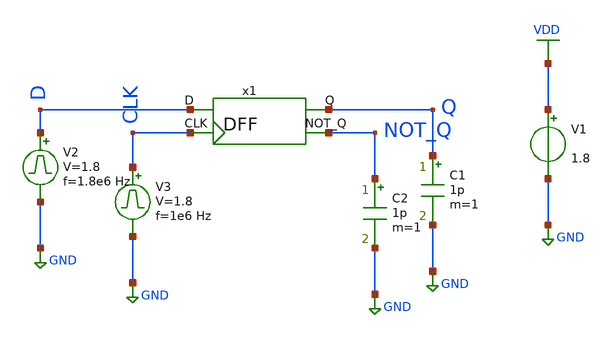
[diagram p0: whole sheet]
** sch_path: library/xschem/DFF_tb.sch
**.subckt DFF_tb
V1 VDD GND 1.8
V2 D GND pulse 0 1.8 '0.495/ 1.8e6 ' '0.01/1.8e6 ' '0.01/1.8e6 ' '0.49/1.8e6 ' '1/1.8e6 '
C1 Q GND 1p m=1
V3 CLK GND pulse 0 1.8 '0.495/ 1e6 ' '0.01/1e6 ' '0.01/1e6 ' '0.49/1e6 ' '1/1e6 '
C2 NOT_Q GND 1p m=1
x1 Q D CLK NOT_Q DFF
**** begin user architecture code


.control
save all
tran 1n 4u
plot V(CLK) V(D)+2 V(Q)+4 V(NOT_Q)+6
.endc


** opencircuitdesign pdks install
.lib $::SKYWATER_MODELS/sky130.lib.spice tt


**** end user architecture code
**.ends

* expanding   symbol:  DFF.sym # of pins=4
** sym_path: library/xschem/DFF.sym
** sch_path: library/xschem/DFF.sch
.subckt DFF Q D CLK NOT_Q
*.ipin D
*.opin Q
*.opin NOT_Q
*.ipin CLK
x1 net2 net1 Q NOT_Q Dlatch
x2 D CLK net2 net3 Dlatch
x3 CLK net1 inv
.ends


* expanding   symbol:  Dlatch.sym # of pins=4
** sym_path: library/xschem/Dlatch.sym
** sch_path: library/xschem/Dlatch.sch
.subckt Dlatch D CLK Q NOT_Q
*.ipin D
*.ipin CLK
*.opin Q
*.opin NOT_Q
XM1 net1 CLK net2 GND sky130_fd_pr__nfet_01v8 L=0.15 W=1 nf=1 ad='int((nf+1)/2) * W/nf * 0.29' as='int((nf+2)/2) * W/nf * 0.29'
+ pd='2*int((nf+1)/2) * (W/nf + 0.29)' ps='2*int((nf+2)/2) * (W/nf + 0.29)' nrd='0.29 / W' nrs='0.29 / W'
+ sa=0 sb=0 sd=0 mult=1 m=1
XM2 net1 D VDD VDD sky130_fd_pr__pfet_01v8 L=0.15 W=1 nf=1 ad='int((nf+1)/2) * W/nf * 0.29' as='int((nf+2)/2) * W/nf * 0.29'
+ pd='2*int((nf+1)/2) * (W/nf + 0.29)' ps='2*int((nf+2)/2) * (W/nf + 0.29)' nrd='0.29 / W' nrs='0.29 / W'
+ sa=0 sb=0 sd=0 mult=1 m=1
XM3 net1 CLK VDD VDD sky130_fd_pr__pfet_01v8 L=0.15 W=1 nf=1 ad='int((nf+1)/2) * W/nf * 0.29' as='int((nf+2)/2) * W/nf * 0.29'
+ pd='2*int((nf+1)/2) * (W/nf + 0.29)' ps='2*int((nf+2)/2) * (W/nf + 0.29)' nrd='0.29 / W' nrs='0.29 / W'
+ sa=0 sb=0 sd=0 mult=1 m=1
XM4 net2 D GND GND sky130_fd_pr__nfet_01v8 L=0.15 W=1 nf=1 ad='int((nf+1)/2) * W/nf * 0.29' as='int((nf+2)/2) * W/nf * 0.29'
+ pd='2*int((nf+1)/2) * (W/nf + 0.29)' ps='2*int((nf+2)/2) * (W/nf + 0.29)' nrd='0.29 / W' nrs='0.29 / W'
+ sa=0 sb=0 sd=0 mult=1 m=1
XM5 Q NOT_Q net3 GND sky130_fd_pr__nfet_01v8 L=0.15 W=1 nf=1 ad='int((nf+1)/2) * W/nf * 0.29' as='int((nf+2)/2) * W/nf * 0.29'
+ pd='2*int((nf+1)/2) * (W/nf + 0.29)' ps='2*int((nf+2)/2) * (W/nf + 0.29)' nrd='0.29 / W' nrs='0.29 / W'
+ sa=0 sb=0 sd=0 mult=1 m=1
XM6 Q net1 VDD VDD sky130_fd_pr__pfet_01v8 L=0.15 W=1 nf=1 ad='int((nf+1)/2) * W/nf * 0.29' as='int((nf+2)/2) * W/nf * 0.29'
+ pd='2*int((nf+1)/2) * (W/nf + 0.29)' ps='2*int((nf+2)/2) * (W/nf + 0.29)' nrd='0.29 / W' nrs='0.29 / W'
+ sa=0 sb=0 sd=0 mult=1 m=1
XM7 Q NOT_Q VDD VDD sky130_fd_pr__pfet_01v8 L=0.15 W=1 nf=1 ad='int((nf+1)/2) * W/nf * 0.29' as='int((nf+2)/2) * W/nf * 0.29'
+ pd='2*int((nf+1)/2) * (W/nf + 0.29)' ps='2*int((nf+2)/2) * (W/nf + 0.29)' nrd='0.29 / W' nrs='0.29 / W'
+ sa=0 sb=0 sd=0 mult=1 m=1
XM8 net3 net1 GND GND sky130_fd_pr__nfet_01v8 L=0.15 W=1 nf=1 ad='int((nf+1)/2) * W/nf * 0.29' as='int((nf+2)/2) * W/nf * 0.29'
+ pd='2*int((nf+1)/2) * (W/nf + 0.29)' ps='2*int((nf+2)/2) * (W/nf + 0.29)' nrd='0.29 / W' nrs='0.29 / W'
+ sa=0 sb=0 sd=0 mult=1 m=1
XM9 NOT_Q net5 net4 GND sky130_fd_pr__nfet_01v8 L=0.15 W=1 nf=1 ad='int((nf+1)/2) * W/nf * 0.29' as='int((nf+2)/2) * W/nf * 0.29'
+ pd='2*int((nf+1)/2) * (W/nf + 0.29)' ps='2*int((nf+2)/2) * (W/nf + 0.29)' nrd='0.29 / W' nrs='0.29 / W'
+ sa=0 sb=0 sd=0 mult=1 m=1
XM10 NOT_Q Q VDD VDD sky130_fd_pr__pfet_01v8 L=0.15 W=1 nf=1 ad='int((nf+1)/2) * W/nf * 0.29' as='int((nf+2)/2) * W/nf * 0.29'
+ pd='2*int((nf+1)/2) * (W/nf + 0.29)' ps='2*int((nf+2)/2) * (W/nf + 0.29)' nrd='0.29 / W' nrs='0.29 / W'
+ sa=0 sb=0 sd=0 mult=1 m=1
XM11 NOT_Q net5 VDD VDD sky130_fd_pr__pfet_01v8 L=0.15 W=1 nf=1 ad='int((nf+1)/2) * W/nf * 0.29' as='int((nf+2)/2) * W/nf * 0.29'
+ pd='2*int((nf+1)/2) * (W/nf + 0.29)' ps='2*int((nf+2)/2) * (W/nf + 0.29)' nrd='0.29 / W' nrs='0.29 / W'
+ sa=0 sb=0 sd=0 mult=1 m=1
XM12 net4 Q GND GND sky130_fd_pr__nfet_01v8 L=0.15 W=1 nf=1 ad='int((nf+1)/2) * W/nf * 0.29' as='int((nf+2)/2) * W/nf * 0.29'
+ pd='2*int((nf+1)/2) * (W/nf + 0.29)' ps='2*int((nf+2)/2) * (W/nf + 0.29)' nrd='0.29 / W' nrs='0.29 / W'
+ sa=0 sb=0 sd=0 mult=1 m=1
XM13 net5 net7 net6 GND sky130_fd_pr__nfet_01v8 L=0.15 W=1 nf=1 ad='int((nf+1)/2) * W/nf * 0.29' as='int((nf+2)/2) * W/nf * 0.29'
+ pd='2*int((nf+1)/2) * (W/nf + 0.29)' ps='2*int((nf+2)/2) * (W/nf + 0.29)' nrd='0.29 / W' nrs='0.29 / W'
+ sa=0 sb=0 sd=0 mult=1 m=1
XM14 net5 CLK VDD VDD sky130_fd_pr__pfet_01v8 L=0.15 W=1 nf=1 ad='int((nf+1)/2) * W/nf * 0.29' as='int((nf+2)/2) * W/nf * 0.29'
+ pd='2*int((nf+1)/2) * (W/nf + 0.29)' ps='2*int((nf+2)/2) * (W/nf + 0.29)' nrd='0.29 / W' nrs='0.29 / W'
+ sa=0 sb=0 sd=0 mult=1 m=1
XM15 net5 net7 VDD VDD sky130_fd_pr__pfet_01v8 L=0.15 W=1 nf=1 ad='int((nf+1)/2) * W/nf * 0.29' as='int((nf+2)/2) * W/nf * 0.29'
+ pd='2*int((nf+1)/2) * (W/nf + 0.29)' ps='2*int((nf+2)/2) * (W/nf + 0.29)' nrd='0.29 / W' nrs='0.29 / W'
+ sa=0 sb=0 sd=0 mult=1 m=1
XM16 net6 CLK GND GND sky130_fd_pr__nfet_01v8 L=0.15 W=1 nf=1 ad='int((nf+1)/2) * W/nf * 0.29' as='int((nf+2)/2) * W/nf * 0.29'
+ pd='2*int((nf+1)/2) * (W/nf + 0.29)' ps='2*int((nf+2)/2) * (W/nf + 0.29)' nrd='0.29 / W' nrs='0.29 / W'
+ sa=0 sb=0 sd=0 mult=1 m=1
XM17 net7 D GND GND sky130_fd_pr__nfet_01v8 L=0.15 W=1 nf=1 ad='int((nf+1)/2) * W/nf * 0.29' as='int((nf+2)/2) * W/nf * 0.29'
+ pd='2*int((nf+1)/2) * (W/nf + 0.29)' ps='2*int((nf+2)/2) * (W/nf + 0.29)' nrd='0.29 / W' nrs='0.29 / W'
+ sa=0 sb=0 sd=0 mult=1 m=1
XM18 net7 D VDD VDD sky130_fd_pr__pfet_01v8 L=0.15 W=1 nf=1 ad='int((nf+1)/2) * W/nf * 0.29' as='int((nf+2)/2) * W/nf * 0.29'
+ pd='2*int((nf+1)/2) * (W/nf + 0.29)' ps='2*int((nf+2)/2) * (W/nf + 0.29)' nrd='0.29 / W' nrs='0.29 / W'
+ sa=0 sb=0 sd=0 mult=1 m=1
.ends


* expanding   symbol:  inv.sym # of pins=2
** sym_path: library/xschem/inv.sym
** sch_path: library/xschem/inv.sch
.subckt inv A Y
*.opin Y
*.ipin A
XM1 Y A GND GND sky130_fd_pr__nfet_01v8 L=0.15 W=1 nf=1 ad='int((nf+1)/2) * W/nf * 0.29' as='int((nf+2)/2) * W/nf * 0.29'
+ pd='2*int((nf+1)/2) * (W/nf + 0.29)' ps='2*int((nf+2)/2) * (W/nf + 0.29)' nrd='0.29 / W' nrs='0.29 / W'
+ sa=0 sb=0 sd=0 mult=1 m=1
XM2 Y A VDD VDD sky130_fd_pr__pfet_01v8 L=0.15 W=1 nf=1 ad='int((nf+1)/2) * W/nf * 0.29' as='int((nf+2)/2) * W/nf * 0.29'
+ pd='2*int((nf+1)/2) * (W/nf + 0.29)' ps='2*int((nf+2)/2) * (W/nf + 0.29)' nrd='0.29 / W' nrs='0.29 / W'
+ sa=0 sb=0 sd=0 mult=1 m=1
.ends

.GLOBAL VDD
.GLOBAL GND
.end
